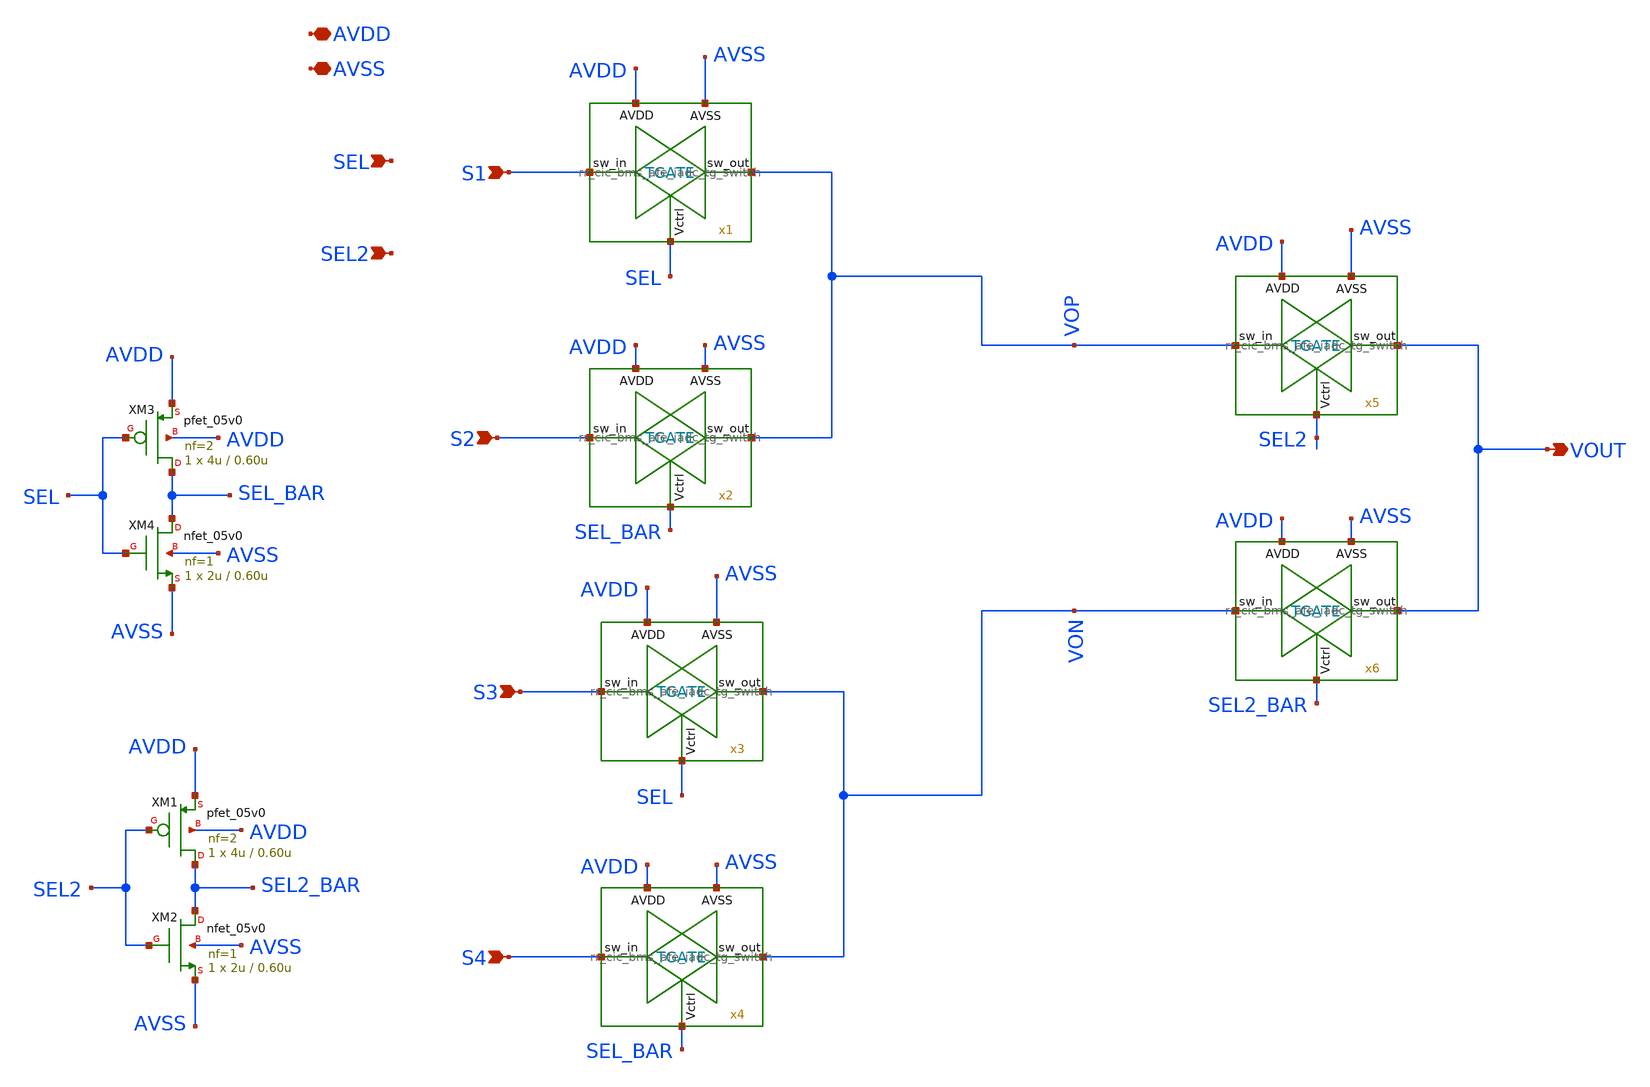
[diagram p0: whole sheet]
** sch_path: design/schematics/MUX/pkr_cic_bms_afe_mux_4x1.sch
**.subckt pkr_cic_bms_afe_mux_4x1 S1 S2 S3 S4 SEL AVDD AVSS VOUT SEL2
*.ipin S1
*.ipin S2
*.ipin S3
*.ipin S4
*.ipin SEL
*.iopin AVDD
*.iopin AVSS
*.opin VOUT
*.ipin SEL2
x1 AVDD SEL S1 VOP AVSS rr_cic_bms_afe_iadc_tg_switch
x2 AVDD SEL_BAR S2 VOP AVSS rr_cic_bms_afe_iadc_tg_switch
x3 AVDD SEL S3 VON AVSS rr_cic_bms_afe_iadc_tg_switch
x4 AVDD SEL_BAR S4 VON AVSS rr_cic_bms_afe_iadc_tg_switch
x5 AVDD SEL2 VOP VOUT AVSS rr_cic_bms_afe_iadc_tg_switch
x6 AVDD SEL2_BAR VON VOUT AVSS rr_cic_bms_afe_iadc_tg_switch
XM3 SEL_BAR SEL AVDD AVDD pfet_05v0 L=0.60u W=4u nf=2 ad='int((nf+1)/2) * W/nf * 0.18u' as='int((nf+2)/2) * W/nf * 0.18u'
+ pd='2*int((nf+1)/2) * (W/nf + 0.18u)' ps='2*int((nf+2)/2) * (W/nf + 0.18u)' nrd='0.18u / W' nrs='0.18u / W'
+ sa=0 sb=0 sd=0 m=1
XM4 SEL_BAR SEL AVSS AVSS nfet_05v0 L=0.60u W=2u nf=1 ad='int((nf+1)/2) * W/nf * 0.18u' as='int((nf+2)/2) * W/nf * 0.18u'
+ pd='2*int((nf+1)/2) * (W/nf + 0.18u)' ps='2*int((nf+2)/2) * (W/nf + 0.18u)' nrd='0.18u / W' nrs='0.18u / W'
+ sa=0 sb=0 sd=0 m=1
XM1 SEL2_BAR SEL2 AVDD AVDD pfet_05v0 L=0.60u W=4u nf=2 ad='int((nf+1)/2) * W/nf * 0.18u' as='int((nf+2)/2) * W/nf * 0.18u'
+ pd='2*int((nf+1)/2) * (W/nf + 0.18u)' ps='2*int((nf+2)/2) * (W/nf + 0.18u)' nrd='0.18u / W' nrs='0.18u / W'
+ sa=0 sb=0 sd=0 m=1
XM2 SEL2_BAR SEL2 AVSS AVSS nfet_05v0 L=0.60u W=2u nf=1 ad='int((nf+1)/2) * W/nf * 0.18u' as='int((nf+2)/2) * W/nf * 0.18u'
+ pd='2*int((nf+1)/2) * (W/nf + 0.18u)' ps='2*int((nf+2)/2) * (W/nf + 0.18u)' nrd='0.18u / W' nrs='0.18u / W'
+ sa=0 sb=0 sd=0 m=1
**.ends

* expanding   symbol:  dsm/dsm/rr_cic_bms_afe_iadc_tg_switch.sym # of pins=5
** sym_path: design/schematics/ADC/DSM_Loop_filter/second_int/Switches+TG+Cap/rr_cic_bms_afe_iadc_tg_switch.sym
** sch_path: design/schematics/ADC/DSM_Loop_filter/second_int/Switches+TG+Cap/rr_cic_bms_afe_iadc_tg_switch.sch
.subckt rr_cic_bms_afe_iadc_tg_switch AVDD Vctrl sw_in sw_out AVSS
*.ipin sw_in
*.opin sw_out
*.ipin Vctrl
*.ipin AVDD
*.ipin AVSS
XM1 sw_in Vctrl sw_out AVSS nfet_05v0 L=0.60u W=1.2u nf=1 ad='int((nf+1)/2) * W/nf * 0.18u' as='int((nf+2)/2) * W/nf * 0.18u'
+ pd='2*int((nf+1)/2) * (W/nf + 0.18u)' ps='2*int((nf+2)/2) * (W/nf + 0.18u)' nrd='0.18u / W' nrs='0.18u / W'
+ sa=0 sb=0 sd=0 m=1
XM2 sw_out Vctrl_b sw_in AVDD pfet_05v0 L=0.50u W=2u nf=2 ad='int((nf+1)/2) * W/nf * 0.18u' as='int((nf+2)/2) * W/nf * 0.18u'
+ pd='2*int((nf+1)/2) * (W/nf + 0.18u)' ps='2*int((nf+2)/2) * (W/nf + 0.18u)' nrd='0.18u / W' nrs='0.18u / W'
+ sa=0 sb=0 sd=0 m=2
XM3 Vctrl_b Vctrl AVDD AVDD pfet_05v0 L=0.60u W=4u nf=2 ad='int((nf+1)/2) * W/nf * 0.18u' as='int((nf+2)/2) * W/nf * 0.18u'
+ pd='2*int((nf+1)/2) * (W/nf + 0.18u)' ps='2*int((nf+2)/2) * (W/nf + 0.18u)' nrd='0.18u / W' nrs='0.18u / W'
+ sa=0 sb=0 sd=0 m=1
XM4 Vctrl_b Vctrl AVSS AVSS nfet_05v0 L=0.60u W=2u nf=1 ad='int((nf+1)/2) * W/nf * 0.18u' as='int((nf+2)/2) * W/nf * 0.18u'
+ pd='2*int((nf+1)/2) * (W/nf + 0.18u)' ps='2*int((nf+2)/2) * (W/nf + 0.18u)' nrd='0.18u / W' nrs='0.18u / W'
+ sa=0 sb=0 sd=0 m=1
.ends

.end
